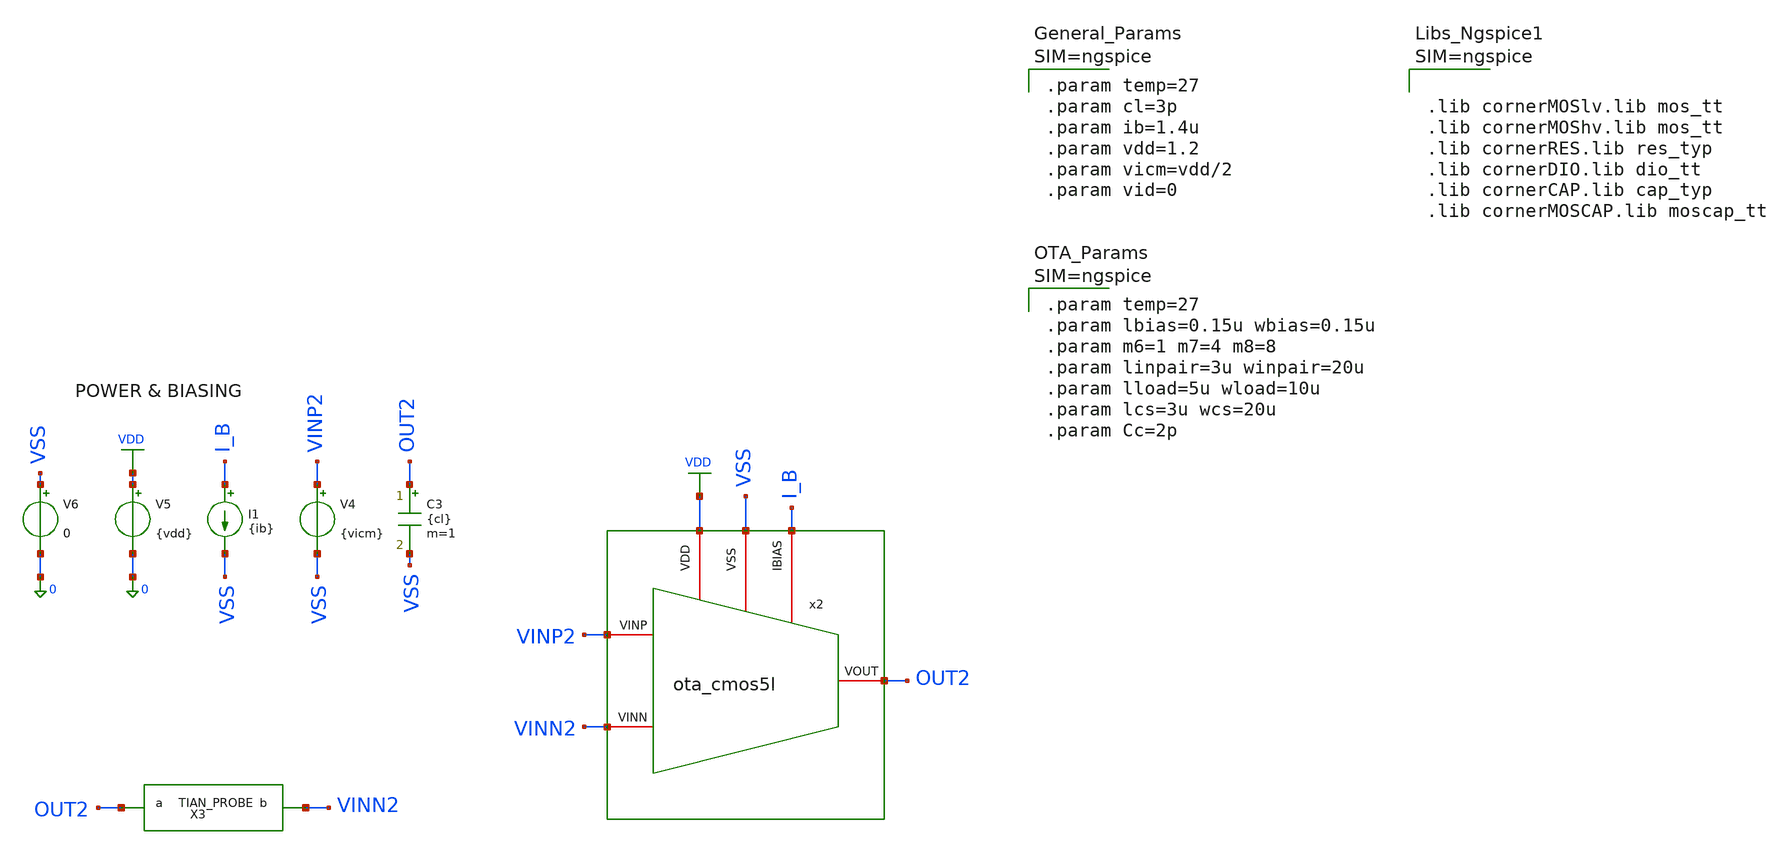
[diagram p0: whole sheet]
** sch_path: xschem/ota_cmos5l/tb/tb_ota_cmos5l_noise/tb_ota_cmos5l_noise.sch
**.subckt tb_ota_cmos5l_noise
I1 I_B VSS {ib}
V5 VDD 0 {vdd}
V6 VSS 0 0
V4 VINP2 VSS {vicm}
C3 OUT2 VSS {cl} m=1
x2 VSS I_B VDD VINN2 VINP2 OUT2 ota_cmos5l
X3 OUT2 VINN2 loopgainprobe
**** begin user architecture code



.lib cornerMOSlv.lib mos_tt
.lib cornerMOShv.lib mos_tt
.lib cornerRES.lib res_typ
.lib cornerDIO.lib dio_tt
.lib cornerCAP.lib cap_typ
.lib cornerMOSCAP.lib moscap_tt





.subckt loopgainprobe a b
Ii 0 x DC 0 AC 0
Vi x a DC 0 AC 1
Vnodebuffer b x 0
.ends loopgainprobe

.func tian_loop() {1/(1/(2*(ac1.i(v.x999.Vi)*ac2.v(x999.x)-ac1.v(x999.x)*ac2.i(v.x999.Vi))+ac1.v(x999.x)+ac2.i(v.x999.Vi))-1)}





.param temp=27
.param cl=3p
.param ib=1.4u
.param vdd=1.2
.param vicm=vdd/2
.param vid=0





.param temp=27
.param lbias=0.15u wbias=0.15u
.param m6=1 m7=4 m8=8
.param linpair=3u winpair=20u
.param lload=5u wload=10u
.param lcs=3u wcs=20u
.param Cc=2p





.control
save all
destroy all
shell mkdir -p result

* Tian probe idled
alter i.x999.ii acmag=0
alter v.x999.vi acmag=0

* Add AC 1 to Vicm
alter @v4[acmag]=1

* Noise simulation
noise v(out2) v4 dec 20 10 100MEG

* Return to initial condition
alter @v4[acmag]=0

setplot noise1

* Parameters #1
let inoise_total_uv = noise2.inoise_total * 1e6
let onoise_total_uv = noise2.onoise_total * 1e6
let irn_nv = noise1.inoise_spectrum * 1e9
let orn_nv = noise1.onoise_spectrum * 1e9

* IRN extraction at certain frequencies
let irn_10 = irn_nv[0]
let irn_100 = irn_nv[20]
let irn_1k = irn_nv[40]
let irn_10k = irn_nv[60]
let irn_100k = irn_nv[80]
let irn_1meg = irn_nv[100]
* meas noise irn_10 find irn_nv at=10
* meas noise irn_100 find irn_nv at=100
* meas noise irn_1k find irn_nv at=1k
* meas noise irn_10k find irn_nv at=10k
* meas noise irn_100k find irn_nv at=100k
* meas noise irn_1meg find irn_nv at=1MEG

write ./result/tb_cg_ota_noise.raw irn_nv orn_nv inoise_spectrum onoise_spectrum

echo "======================================================="
echo " Total Output Noise (10 Hz - 100 MHz): " $&onoise_total_uv " uV_rms"
echo " Total Input Noise (10 Hz - 100 MHz): " $&inoise_total_uv " uV_rms"
echo "-------------------------------------------------------"
echo " IRN @ 10 Hz (Flicker Noise): " $&irn_10 " nV/sqrt(Hz)"
echo " IRN @ 100 Hz: " $&irn_100 " nV/sqrt(Hz)"
echo " IRN @ 1 kHz: " $&irn_1k " nV/sqrt(Hz)"
echo " IRN @ 10 kHz: " $&irn_10k " nV/sqrt(Hz)"
echo " IRN @ 100 kHz: " $&irn_100k " nV/sqrt(Hz)"
echo " IRN @ 1 MHz (Thermal Noise Floor): " $&irn_1meg " nV/sqrt(Hz)"
echo "======================================================="

.endc



**** end user architecture code
**.ends

* expanding   symbol:  /foss/designs/sg13cmos5l_spma_ip__instramp/xschem/ota_cmos5l/ota_cmos5l.sym #
*+ of pins=6
** sym_path: xschem/output_buffer/ota_cmos5l.sym
** sch_path: xschem/output_buffer/ota_cmos5l.sch
.subckt ota_cmos5l VSS IBIAS VDD VINN VINP VOUT
*.iopin IBIAS
*.iopin VDD
*.iopin VSS
*.iopin VOUT
*.iopin VINP
*.iopin VINN
XM6 IBIAS IBIAS VDD VDD sg13_lv_pmos w={wbias} l={lbias} ng=1 m={m6} mm_ok=1
XM7 net1 IBIAS VDD VDD sg13_lv_pmos w={wbias} l={lbias} ng=1 m={m7} mm_ok=1
XM8 VOUT IBIAS VDD VDD sg13_lv_pmos w={wbias} l={lbias} ng=1 m={m8} mm_ok=1
XM1 net2 VINN net1 VDD sg13_lv_pmos w={winpair} l={linpair} ng=1 m=1 mm_ok=1
XM2 net3 VINP net1 VDD sg13_lv_pmos w={winpair} l={linpair} ng=1 m=1 mm_ok=1
XM3 net2 net2 VSS VSS sg13_lv_nmos w={wload} l={lload} ng=1 m=1 mm_ok=1
XM4 net3 net2 VSS VSS sg13_lv_nmos w={wload} l={lload} ng=1 m=1 mm_ok=1
XM5 VOUT net3 VSS VSS sg13_lv_nmos w={wcs} l={lcs} ng=1 m=1 mm_ok=1
XR1 net3 net4 VSS rhigh w=0.5e-6 l=1.95e-6 m=1 b=0 mm_ok=1
.save v(vinp)
.save v(vinn)
.save v(vout)
XC2 VOUT net4 cap_cmomi w=15e-6 l=15e-6 mmin=1 mmax=4 feed=double subblock=0 m=5 mm_ok=1
**** begin user architecture code


.param temp=27
.param lbias=0.15u wbias=0.15u
.param m6=1 m7=4 m8=8
.param linpair=3u winpair=20u
.param lload=5u wload=10u
.param lcs=3u wcs=20u
.param Cc=2p



**** end user architecture code
XC1 VOUT net4 cap_cmomi w=15e-6 l=15e-6 mmin=1 mmax=4 feed=double subblock=0 m=4 mm_ok=1
.ends

.GLOBAL VDD
.end
